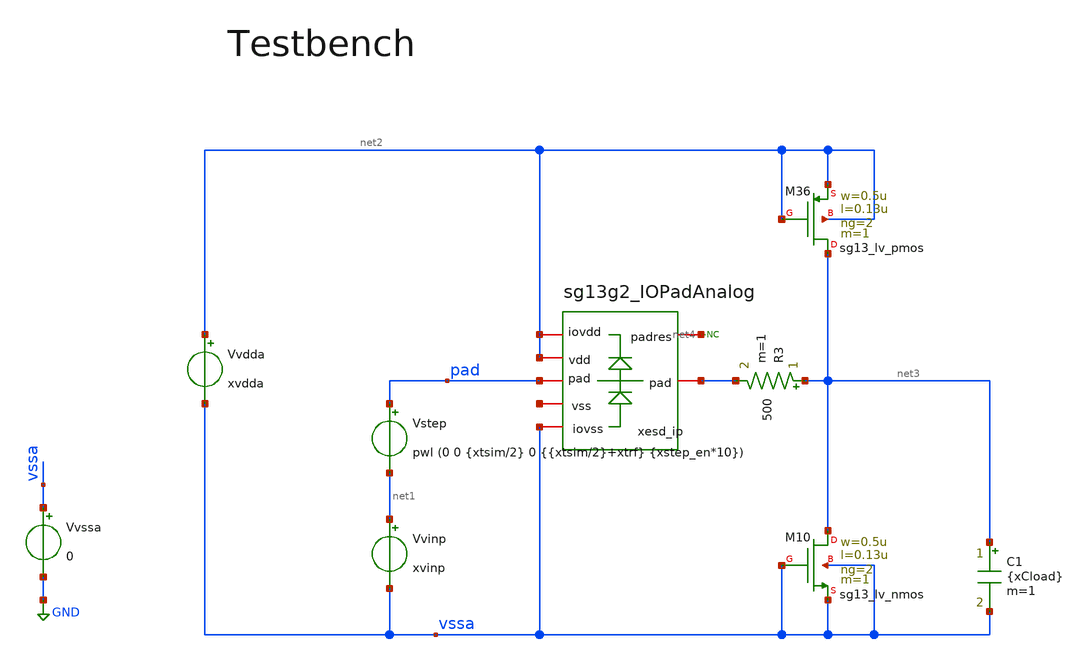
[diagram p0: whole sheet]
** sch_path: tb_OTA_1stage_ihp/tb_OTA_noPEX_iprb.sch
**.subckt tb_OTA_noPEX_iprb
Vstep pad net1 pwl (0 0 {xtsim/2} 0 {{xtsim/2}+xtrf} {xstep_en*10})
Vvinp net1 vssa xvinp
Vvssa vssa GND 0
* noconn #net4
xesd_ip net2 vssa net4 net2 pad net5 sg13g2_IOPadAnalog
Vvdda net2 vssa xvdda
XM10 net3 vssa vssa vssa sg13_lv_nmos w=0.5u l=0.13u ng=2 m=1 mm_ok=1
XM36 net3 net2 net2 net2 sg13_lv_pmos w=0.5u l=0.13u ng=2 m=1 mm_ok=1
C1 net3 vssa {xCload} m=1
R3 net3 pad 500 m=1
**** begin user architecture code

** opencircuitdesign pdks install
.lib /home/slice/pdk/iHP/IHP-Open-PDK/ihp-sg13g2/libs.tech/ngspice/models/cornerMOSlv.lib mos_tt
*.lib /home/slice/pdk/iHP/IHP-Open-PDK/ihp-sg13g2/libs.tech/ngspice/models/sg13g2_moshv_mod.lib
.lib /home/slice/pdk/iHP/IHP-Open-PDK/ihp-sg13g2/libs.tech/ngspice/models/cornerMOShv.lib mos_tt
.lib /home/slice/pdk/iHP/IHP-Open-PDK/ihp-sg13g2/libs.tech/ngspice/models/cornerRES.lib res_typ
.include /home/slice/pdk/iHP/IHP-Open-PDK/ihp-sg13g2/libs.tech/ngspice/models/diodes.lib
*.lib /home/slice/xschem/tb_OTA_1stage_ihp/cornerRES.lib res_typ
*.lib /home/slice/xschem/tb_OTA_1stage_ihp/resistors_mod.lib

*.model
*+ /home/slice/pdk/iHP/IHP-Open-PDK/ihp-sg13g2/libs.tech/ngspice/models/sg13g2_moshv_mod.lib/sg13_hv_pmos

*.model /home/slice/Desktop/acm2/MOSFET_model/Verilog-A/NMOS_ACM_2V0.va
*.model /home/slice/Desktop/acm2/MOSFET_model/Verilog-A/PMOS_ACM_2V0.va

* Parameters
.param xvdda = 1.8
.param xvinp = 1
.param xibias = 40u
.param xCload = 0.75p
.param xCpad = 100f
.param xgm_dp = 1e-3
.param xRin = 1/xgm_dp
.param xCout = 1p
.param xRout = 1e6
.param xtrf = 50p
.param xtsim = 5u
.csparam xtsim_var = 'xtsim'
.param xstep_en = 1

* vlogA instantiation
.model OTA_vcvs OTA_vcvs


  ** must save the below for DCOP analysis to be back annotated onto the schematic
  .option savecurrents

  .include tb_OTA.save
  .save all
  .save v(vout) v(vinp) v(vfb) v(vdda) v(xota.pdio) v(xota.vtail) v(vout_pad)
  .save i(v.xota.Virhs) i(v.xota.Vitail) i(xota.vdda) i(v.Vdda) i(xesd_ip.pad) i(v.Vstep)
  .save i(@n.xota.xm6.nsg13_lv_pmos[ids])


  .control
  let xtsim = $&xtsim_var
  pre_osdi OTA_vcvs.osdi
  save all

** 1. DCOP ANALYSIS **

  op
 * set filetype=ascii
  remzerovec
  write tb_OTA_op.raw

** 2. TRAN ANALYSIS **

  tran 1n $&xtsim
  echo --
  echo TSIM VALUE
    echo $&xtsim
    echo --
  *set filetype=ascii
  remzerovec
  write tb_OTA_tran.raw



  setplot
*quit 0
.endc




**** end user architecture code
**.ends
.GLOBAL GND
.end
